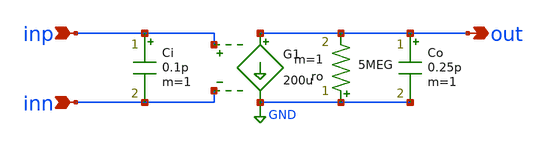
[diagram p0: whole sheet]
** sch_path: prj/template/2_Idealized_circuits/ota_gm_100u_se.sch
**.subckt ota_gm_100u_se inp inn out
*.ipin inp
*.ipin inn
*.opin out
Co out GND 0.25p m=1
ro GND out 5MEG m=1
G1 out GND inp inn 200u
Ci inp inn 0.1p m=1
**.ends
.GLOBAL GND
.end
